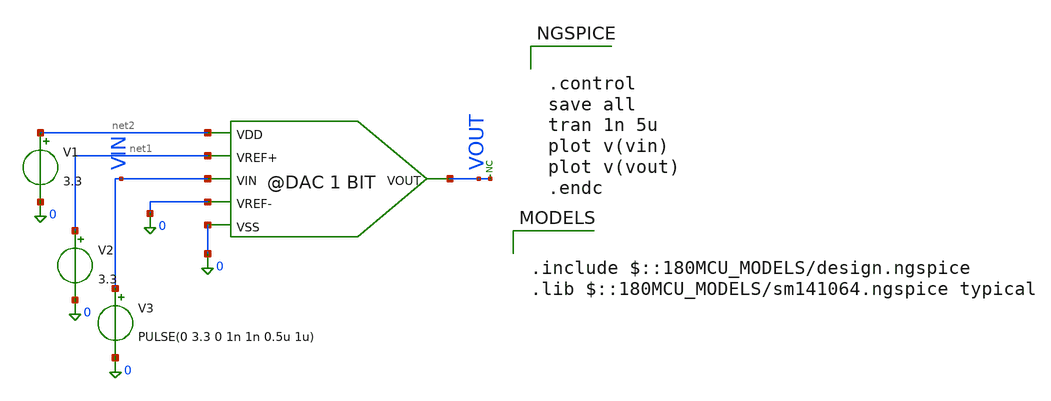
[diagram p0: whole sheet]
** sch_path: src/schematics/dac1bit/DAC_1_BIT_TB.sch
**.subckt DAC_1_BIT_TB
V1 net2 0 3.3
V2 net1 0 3.3
V3 VIN 0 PULSE(0 3.3 0 1n 1n 0.5u 1u)
* noconn VOUT
**** begin user architecture code


.control
save all
tran 1n 5u
plot v(vin)
plot v(vout)
.endc




.include $::180MCU_MODELS/design.ngspice
.lib $::180MCU_MODELS/sm141064.ngspice typical

**** end user architecture code
**.ends
.end
